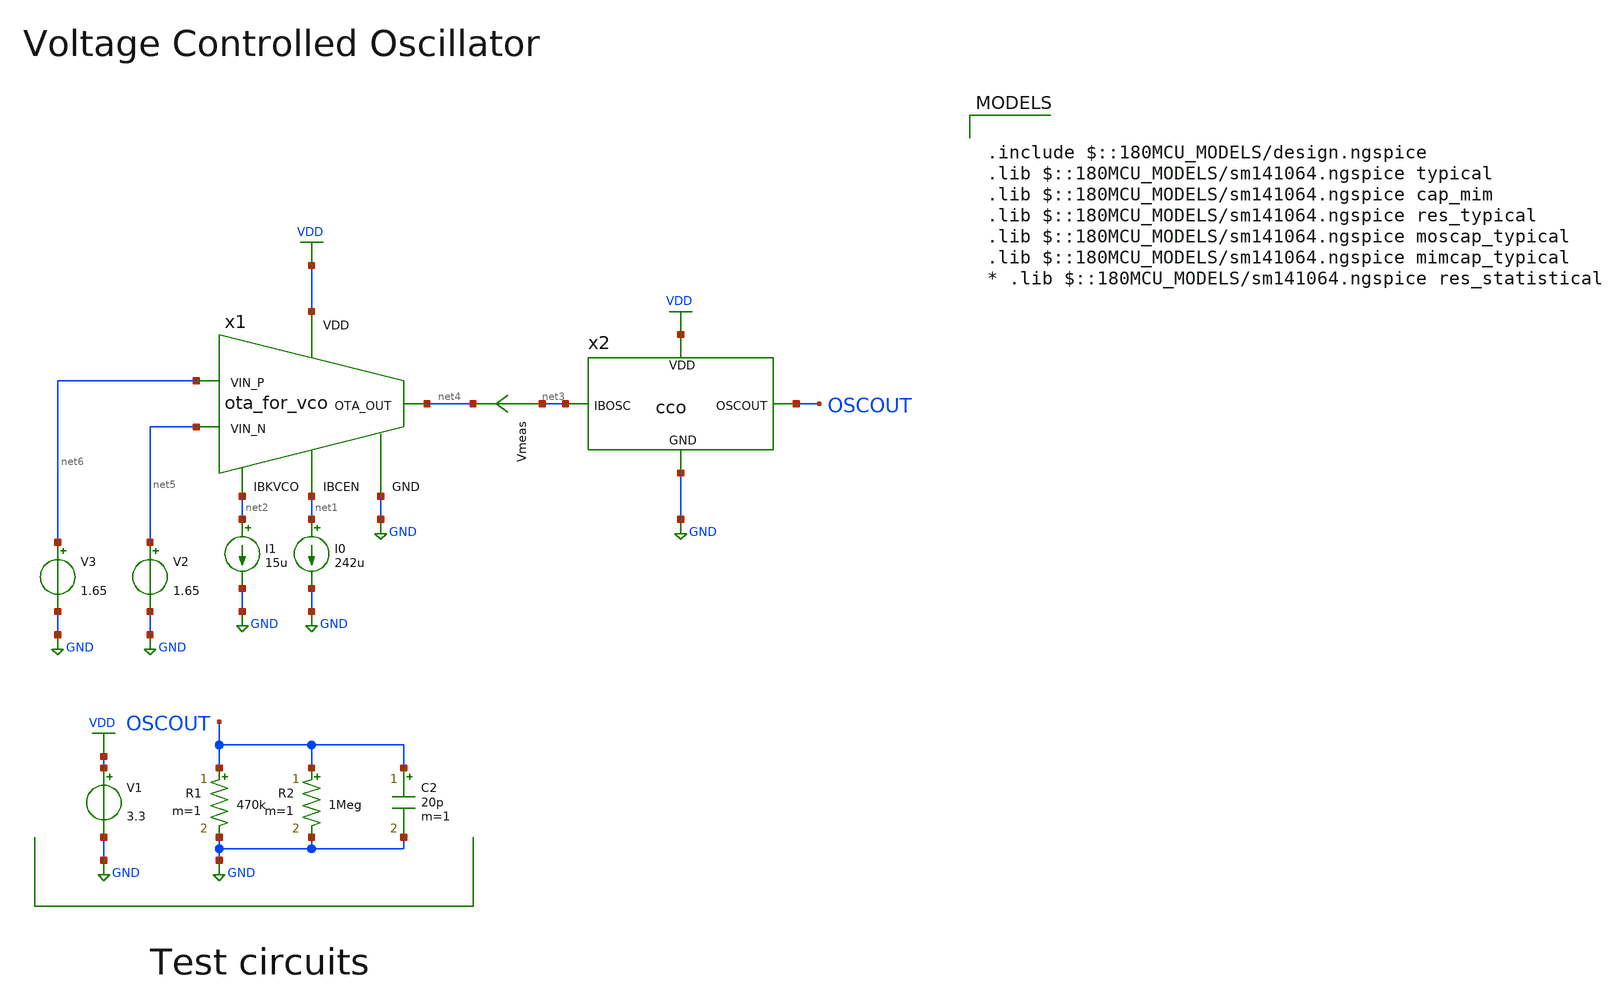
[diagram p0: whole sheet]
** sch_path: designs/libs/tb_analog/tb_vco/tb_vco_tran.sch
* Copyright 2022 GlobalFoundries PDK Authors
* Licensed under the Apache License, Version 2.0 (the "License");
* you may not use this file except in compliance with the License.
* You may obtain a copy of the License at
* https://www.apache.org/licenses/LICENSE-2.0
* Unless required by applicable law or agreed to in writing, software
* distributed under the License is distributed on an "AS IS" BASIS,
* WITHOUT WARRANTIES OR CONDITIONS OF ANY KIND, either express or implied.
* See the License for the specific language governing permissions and
* limitations under the License.
**.subckt tb_vco_tran
V1 VDD GND 3.3
I0 net1 GND 242u
R1 OSCOUT GND 470k m=1
R2 OSCOUT GND 1Meg m=1
C2 OSCOUT GND 20p m=1
x2 VDD GND net3 OSCOUT cco
x1 net2 net5 net6 net4 GND VDD net1 ota_for_vco
I1 net2 GND 15u
Vmeas net3 net4 0
.save i(vmeas)
V2 net5 GND 1.65
V3 net6 GND 1.65
**** begin user architecture code


.control
save all
save currents
let vin=0
let vin_step=0.1
let vin_max=3.3
let count=0
let count_length=((vin_max-vin)/vin_step)
echo count_length:$&count_length
let chart_y_freq=vector(count_length)*0
let chart_x_vin=vector(count_length)*0
settype frequency chart_y_freq
settype voltage chart_x_vin
while const.vin <= const.vin_max
 alter V3=const.vin
 tran   0.04n 0.4u
 plot V(OSCOUT)
 let tdiff=0
 meas tran tdiff TRIG v(OSCOUT) VAL=1.65 RISE=2 TARG v(OSCOUT) VAL=1.65 RISE=3
 if tdiff <> 0
   let freq=1/tdiff
   let const.chart_y_freq[count]=freq
   let const.chart_x_vin[count]=const.vin
 else
   let freq=0
 end

 let const.vin=const.vin+const.vin_step
 let const.count=const.count + 1
end
set nolegend
write tb_vco_tran.raw
setplot new
let frequency_out=const.chart_y_freq
let vco_vin=const.chart_x_vin
setscale vco_vin
set curplotname='freq'
display
set wr_vecnames               ; for wrdata: write the vector names
write tb_vco_freq.raw frequency_out
wrdata tb_vco_freq.txt frequency_out
.endc



.include $::180MCU_MODELS/design.ngspice
.lib $::180MCU_MODELS/sm141064.ngspice typical
.lib $::180MCU_MODELS/sm141064.ngspice cap_mim
.lib $::180MCU_MODELS/sm141064.ngspice res_typical
.lib $::180MCU_MODELS/sm141064.ngspice moscap_typical
.lib $::180MCU_MODELS/sm141064.ngspice mimcap_typical
* .lib $::180MCU_MODELS/sm141064.ngspice res_statistical

**** end user architecture code
**.ends
.GLOBAL VDD
.GLOBAL GND
.end
